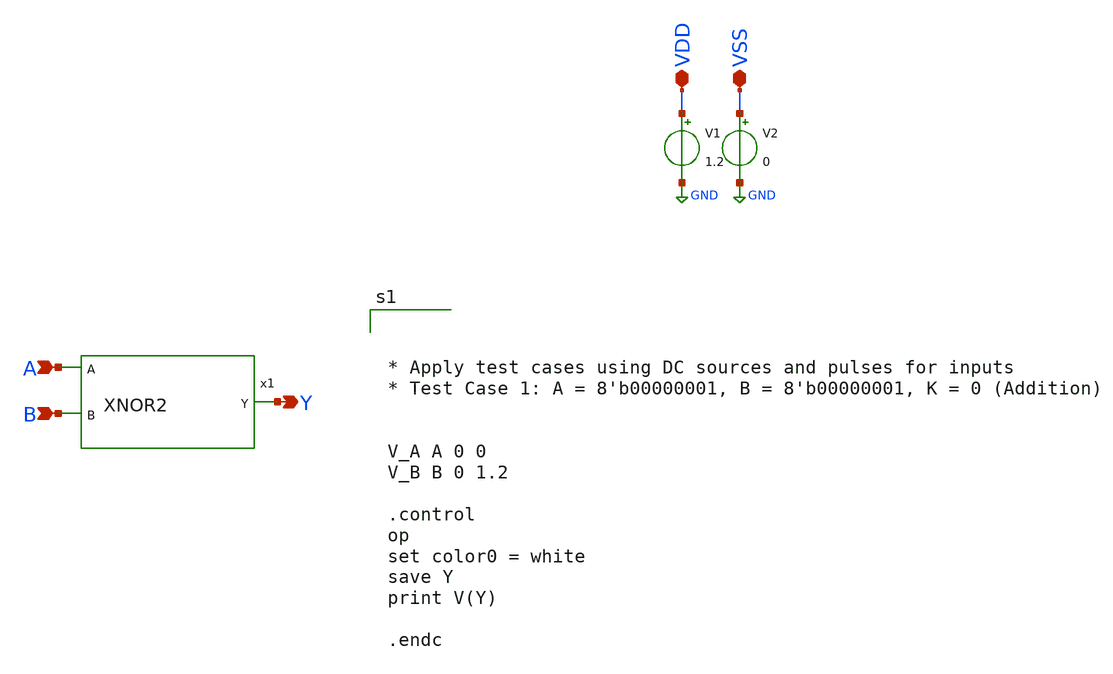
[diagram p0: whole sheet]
** sch_path: design/xschem/TEST_BENCHES/XNOR2_TB.sch
**.subckt XNOR2_TB VDD VSS A B Y
*.iopin VDD
*.iopin VSS
*.ipin A
*.ipin B
*.opin Y
V1 VDD GND 1.2
V2 VSS GND 0
x1 A B Y VSS VDD XNOR2
**** begin user architecture code

** opencircuitdesign pdks install
.lib $::SKYWATER_MODELS/sky130.lib.spice tt_mm





* Apply test cases using DC sources and pulses for inputs
* Test Case 1: A = 8'b00000001, B = 8'b00000001, K = 0 (Addition)


V_A A 0 0
V_B B 0 1.2

.control
op
set color0 = white
save Y
print V(Y)

.endc


**** end user architecture code
**.ends

* expanding   symbol:  XNOR/XNOR2.sym # of pins=3
** sym_path: design/xschem/XNOR/XNOR2.sym
** sch_path: design/xschem/XNOR/XNOR2.sch
.subckt XNOR2 A B Y VSS VDD
*.ipin A
*.ipin B
*.opin Y
x2 A !B B !A Y A !A !B B VSS VDD cg4
x3 A VSS VDD !A inv
x4 B VSS VDD !B inv
.ends


* expanding   symbol:  ./CG4/cg4.sym # of pins=9
** sym_path: design/xschem/CG4/cg4.sym
** sch_path: design/xschem/CG4/cg4.sch
.subckt cg4 P3 P4 P2 P1 OUT N2 N1 N4 N3 VSS VDD
*.ipin P3
*.ipin P1
*.ipin N1
*.ipin N3
*.ipin P4
*.ipin P2
*.ipin N2
*.ipin N4
*.opin OUT
XM1 OUT N1 net1 VSS sky130_fd_pr__nfet_01v8 L=0.15 W=2 nf=1 ad='int((nf+1)/2) * W/nf * 0.29' as='int((nf+2)/2) * W/nf * 0.29'
+ pd='2*int((nf+1)/2) * (W/nf + 0.29)' ps='2*int((nf+2)/2) * (W/nf + 0.29)' nrd='0.29 / W' nrs='0.29 / W'
+ sa=0 sb=0 sd=0 mult=1 m=1
XM2 OUT N2 net2 VSS sky130_fd_pr__nfet_01v8 L=0.15 W=2 nf=1 ad='int((nf+1)/2) * W/nf * 0.29' as='int((nf+2)/2) * W/nf * 0.29'
+ pd='2*int((nf+1)/2) * (W/nf + 0.29)' ps='2*int((nf+2)/2) * (W/nf + 0.29)' nrd='0.29 / W' nrs='0.29 / W'
+ sa=0 sb=0 sd=0 mult=1 m=1
XM3 net1 N3 VSS VSS sky130_fd_pr__nfet_01v8 L=0.15 W=2 nf=1 ad='int((nf+1)/2) * W/nf * 0.29' as='int((nf+2)/2) * W/nf * 0.29'
+ pd='2*int((nf+1)/2) * (W/nf + 0.29)' ps='2*int((nf+2)/2) * (W/nf + 0.29)' nrd='0.29 / W' nrs='0.29 / W'
+ sa=0 sb=0 sd=0 mult=1 m=1
XM4 net2 N4 VSS VSS sky130_fd_pr__nfet_01v8 L=0.15 W=2 nf=1 ad='int((nf+1)/2) * W/nf * 0.29' as='int((nf+2)/2) * W/nf * 0.29'
+ pd='2*int((nf+1)/2) * (W/nf + 0.29)' ps='2*int((nf+2)/2) * (W/nf + 0.29)' nrd='0.29 / W' nrs='0.29 / W'
+ sa=0 sb=0 sd=0 mult=1 m=1
XM5 OUT P1 net3 VDD sky130_fd_pr__pfet_01v8 L=0.15 W=8.25 nf=1 ad='int((nf+1)/2) * W/nf * 0.29' as='int((nf+2)/2) * W/nf * 0.29'
+ pd='2*int((nf+1)/2) * (W/nf + 0.29)' ps='2*int((nf+2)/2) * (W/nf + 0.29)' nrd='0.29 / W' nrs='0.29 / W'
+ sa=0 sb=0 sd=0 mult=1 m=1
XM6 OUT P2 net3 VDD sky130_fd_pr__pfet_01v8 L=0.15 W=8.25 nf=1 ad='int((nf+1)/2) * W/nf * 0.29' as='int((nf+2)/2) * W/nf * 0.29'
+ pd='2*int((nf+1)/2) * (W/nf + 0.29)' ps='2*int((nf+2)/2) * (W/nf + 0.29)' nrd='0.29 / W' nrs='0.29 / W'
+ sa=0 sb=0 sd=0 mult=1 m=1
XM7 net3 P3 VDD VDD sky130_fd_pr__pfet_01v8 L=0.15 W=8.25 nf=1 ad='int((nf+1)/2) * W/nf * 0.29' as='int((nf+2)/2) * W/nf * 0.29'
+ pd='2*int((nf+1)/2) * (W/nf + 0.29)' ps='2*int((nf+2)/2) * (W/nf + 0.29)' nrd='0.29 / W' nrs='0.29 / W'
+ sa=0 sb=0 sd=0 mult=1 m=1
XM8 net3 P4 VDD VDD sky130_fd_pr__pfet_01v8 L=0.15 W=8.25 nf=1 ad='int((nf+1)/2) * W/nf * 0.29' as='int((nf+2)/2) * W/nf * 0.29'
+ pd='2*int((nf+1)/2) * (W/nf + 0.29)' ps='2*int((nf+2)/2) * (W/nf + 0.29)' nrd='0.29 / W' nrs='0.29 / W'
+ sa=0 sb=0 sd=0 mult=1 m=1
.ends


* expanding   symbol:  ./INV/inv.sym # of pins=2
** sym_path: design/xschem/INV/inv.sym
** sch_path: design/xschem/INV/inv.sch
.subckt inv A VSS VDD Y
*.ipin A
*.opin Y
XM2 Y A VSS GND sky130_fd_pr__nfet_01v8 L=0.15 W=1 nf=1 ad='int((nf+1)/2) * W/nf * 0.29' as='int((nf+2)/2) * W/nf * 0.29'
+ pd='2*int((nf+1)/2) * (W/nf + 0.29)' ps='2*int((nf+2)/2) * (W/nf + 0.29)' nrd='0.29 / W' nrs='0.29 / W'
+ sa=0 sb=0 sd=0 mult=1 m=1
XM1 Y A VDD VDD sky130_fd_pr__pfet_01v8 L=0.15 W=3.21 nf=1 ad='int((nf+1)/2) * W/nf * 0.29' as='int((nf+2)/2) * W/nf * 0.29'
+ pd='2*int((nf+1)/2) * (W/nf + 0.29)' ps='2*int((nf+2)/2) * (W/nf + 0.29)' nrd='0.29 / W' nrs='0.29 / W'
+ sa=0 sb=0 sd=0 mult=1 m=1
.ends

.GLOBAL GND
.end
